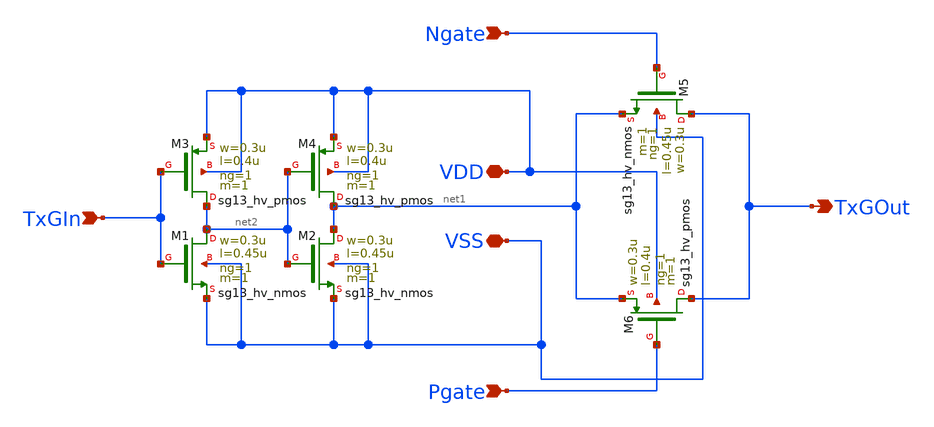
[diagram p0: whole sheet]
** sch_path: circuit_files/sar_adc_20260903/TxGate.sch
**.subckt TxGate Ngate Pgate TxGIn TxGOut VDD VSS
*.ipin Ngate
*.ipin Pgate
*.ipin TxGIn
*.opin TxGOut
*.iopin VDD
*.iopin VSS
XM5 TxGOut Ngate net1 VSS sg13_hv_nmos w=0.3u l=0.45u ng=1 m=1 mm_ok=1
XM1 net2 TxGIn VSS VSS sg13_hv_nmos w=0.3u l=0.45u ng=1 m=1 mm_ok=1
XM2 net1 net2 VSS VSS sg13_hv_nmos w=0.3u l=0.45u ng=1 m=1 mm_ok=1
XM3 net2 TxGIn VDD VDD sg13_hv_pmos w=0.3u l=0.4u ng=1 m=1 mm_ok=1
XM4 net1 net2 VDD VDD sg13_hv_pmos w=0.3u l=0.4u ng=1 m=1 mm_ok=1
XM6 TxGOut Pgate net1 VDD sg13_hv_pmos w=0.3u l=0.4u ng=1 m=1 mm_ok=1
**.ends
.end
